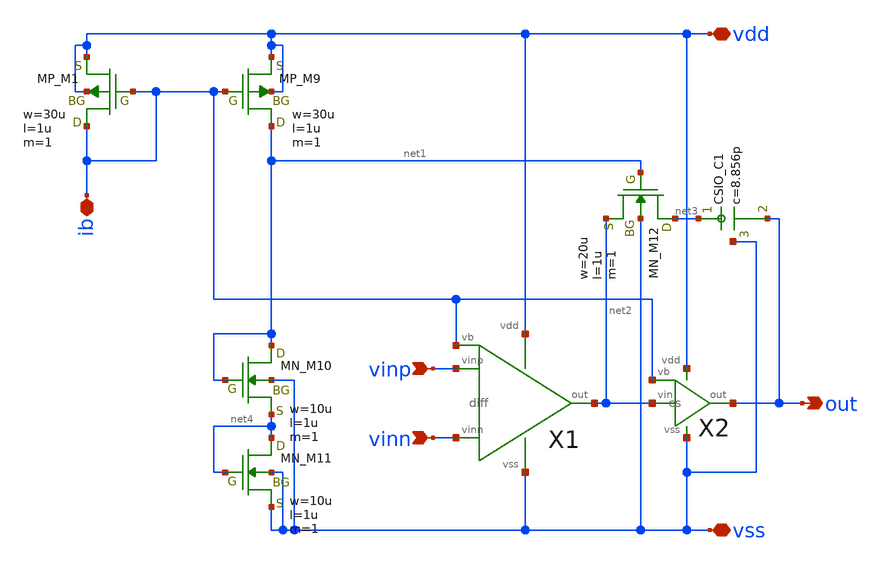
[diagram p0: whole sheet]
** sch_path: OpenSUSI-TR10/opamp/opamp.sch
**.subckt opamp vinp vinn out vdd vss ib
*.ipin vinp
*.ipin vinn
*.opin out
*.iopin vdd
*.iopin vss
*.iopin ib
X1 vinp vinn net2 vdd vss ib diff
X2 net2 ib out vdd vss cs
XM9 net1 ib vdd vdd PMOS w=30u l=1u as=0 ad=0 ps=0 pd=0 nrd=0 nrs=0 m=1
XM12 net3 net1 net2 vss NMOS w=20u l=1u as=0 ad=0 ps=0 pd=0 nrd=0 nrs=0 m=1
XM1 ib ib vdd vdd PMOS w=30u l=1u as=0 ad=0 ps=0 pd=0 nrd=0 nrs=0 m=1
XM10 net1 net1 net4 vss NMOS w=10u l=1u as=0 ad=0 ps=0 pd=0 nrd=0 nrs=0 m=1
XM11 net4 net4 vss vss NMOS w=10u l=1u as=0 ad=0 ps=0 pd=0 nrd=0 nrs=0 m=1
XC1 net3 out vss F_CSIO c=8.856p x=120u y=120u m=1
**.ends

* expanding   symbol:  diff.sym # of pins=6
** sym_path: diff.sym
** sch_path: diff.sch
.subckt diff vinp vinn out vdd vss vb
*.ipin vinn
*.ipin vinp
*.ipin vb
*.opin out
*.iopin vdd
*.iopin vss
M5 net2 vb vdd vdd pmos L=2u W=40u m=1
M1 net1 vinn net2 net2 pmos L=2u W=200u m=1
M2 out vinp net2 net2 pmos L=2u W=200u m=1
M3 net1 net1 vss vss nmos L=2u W=10u m=1
M4 out net1 vss vss nmos L=2u W=10u m=1
.ends


* expanding   symbol:  cs.sym # of pins=5
** sym_path: cs.sym
** sch_path: cs.sch
.subckt cs vin vb out vdd vss
*.ipin vb
*.ipin vin
*.opin out
*.iopin vss
*.iopin vdd
XM6 out vb vdd vdd PMOS w=270u l=1u as=0 ad=0 ps=0 pd=0 nrd=0 nrs=0 m=1
XM7 out vin vss vss NMOS w=90u l=1u as=0 ad=0 ps=0 pd=0 nrd=0 nrs=0 m=1
.ends

.end
